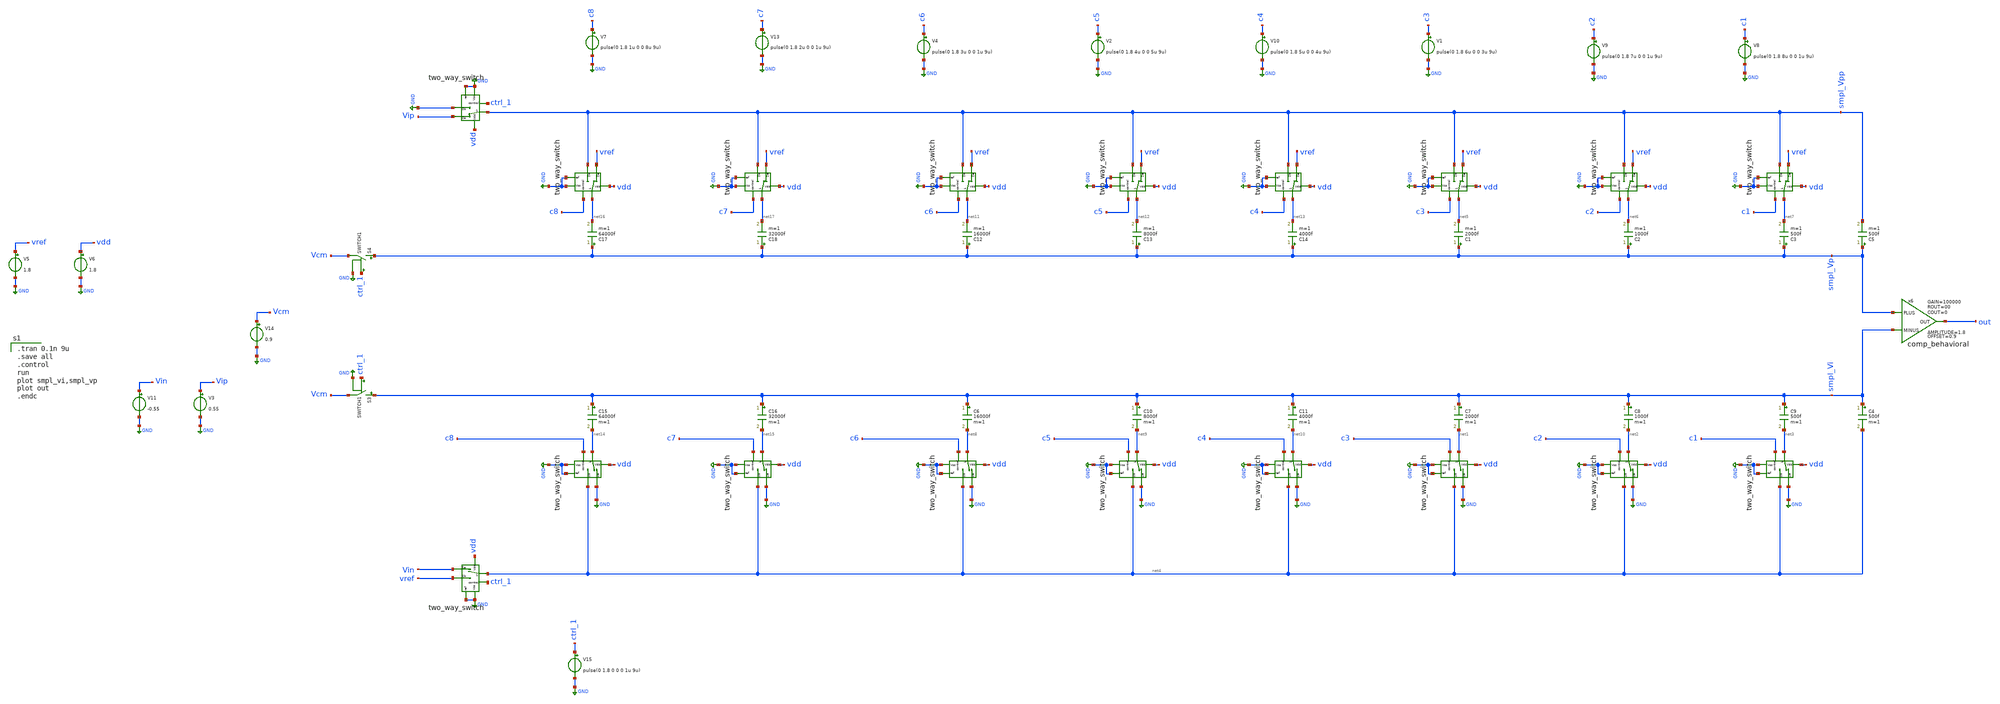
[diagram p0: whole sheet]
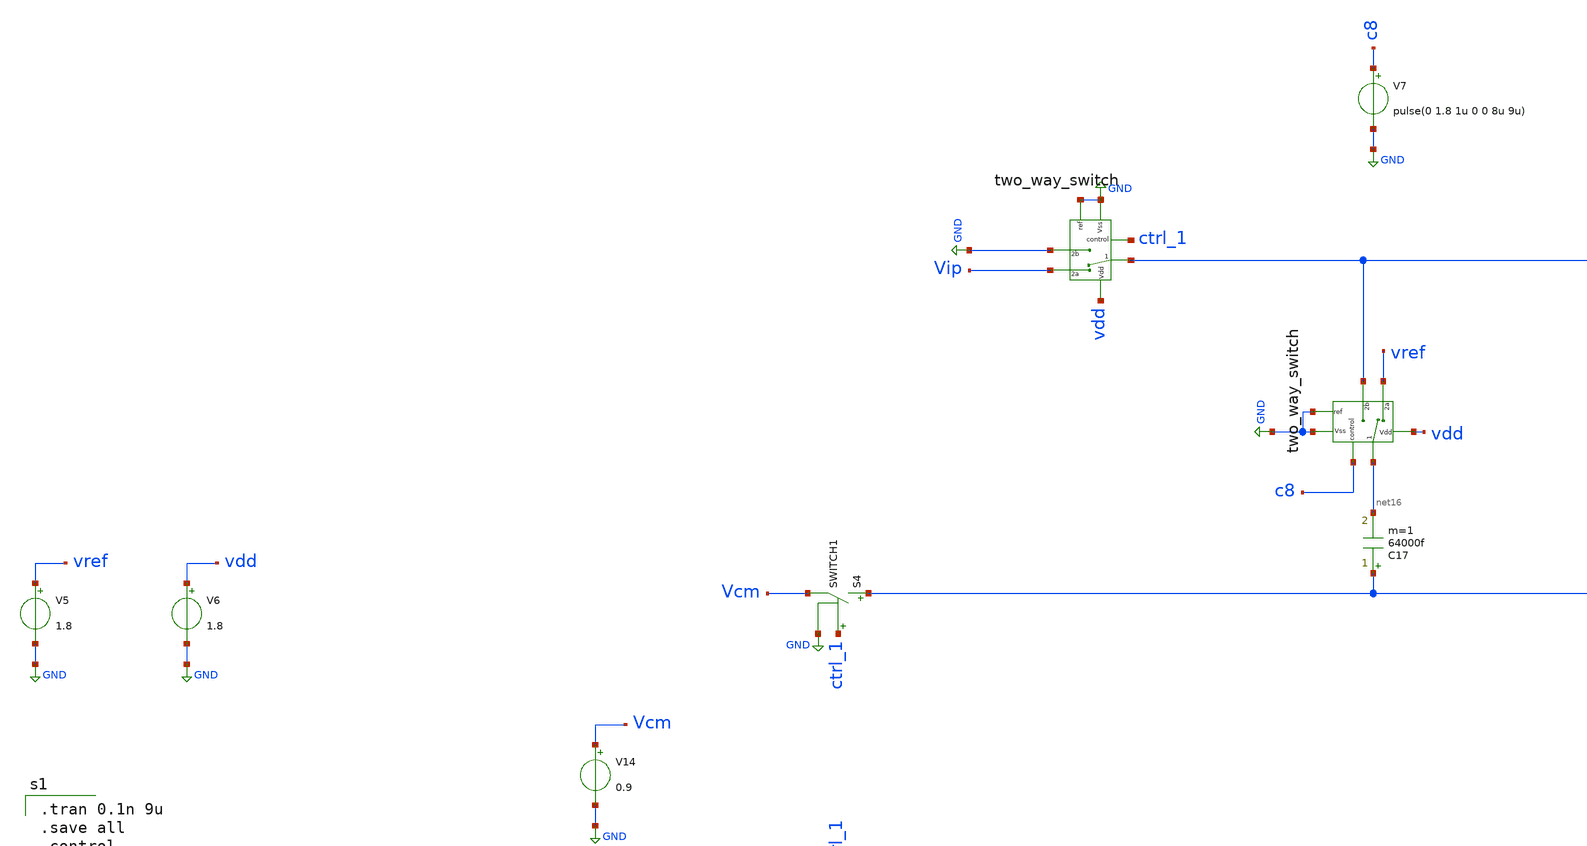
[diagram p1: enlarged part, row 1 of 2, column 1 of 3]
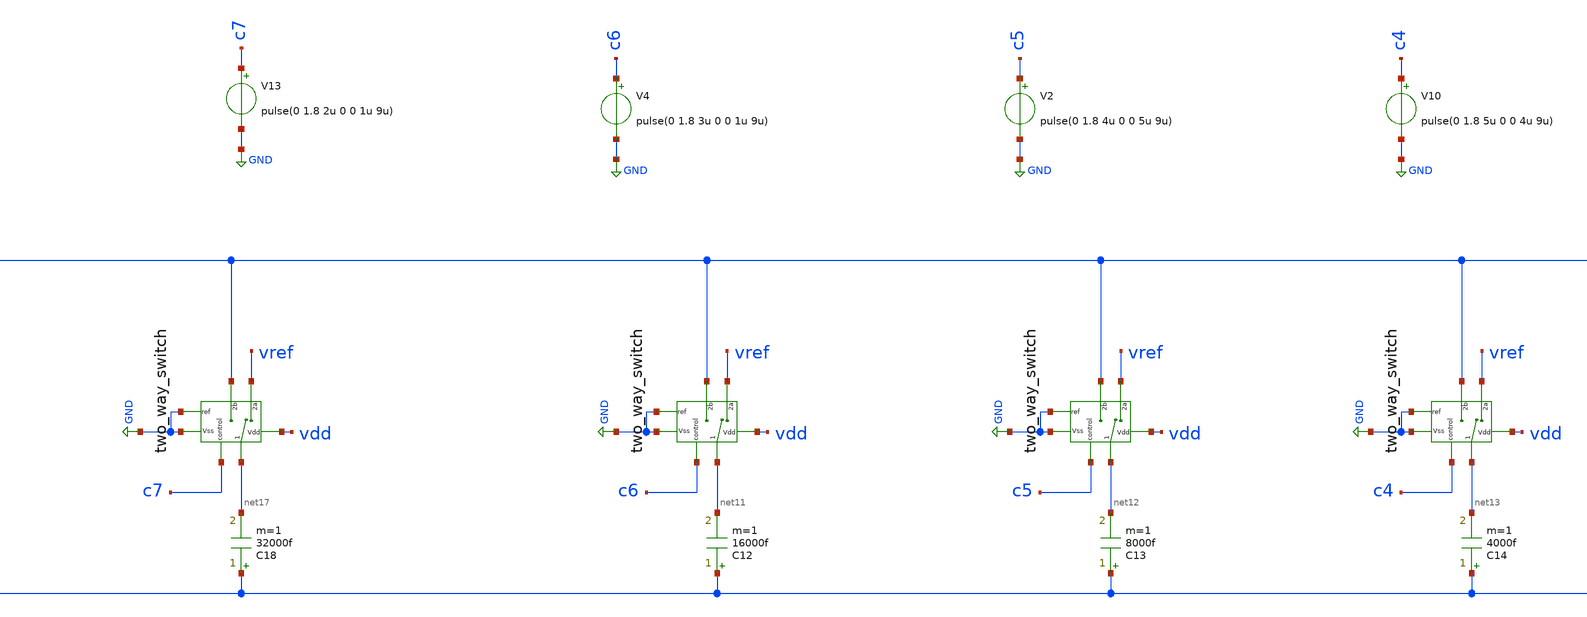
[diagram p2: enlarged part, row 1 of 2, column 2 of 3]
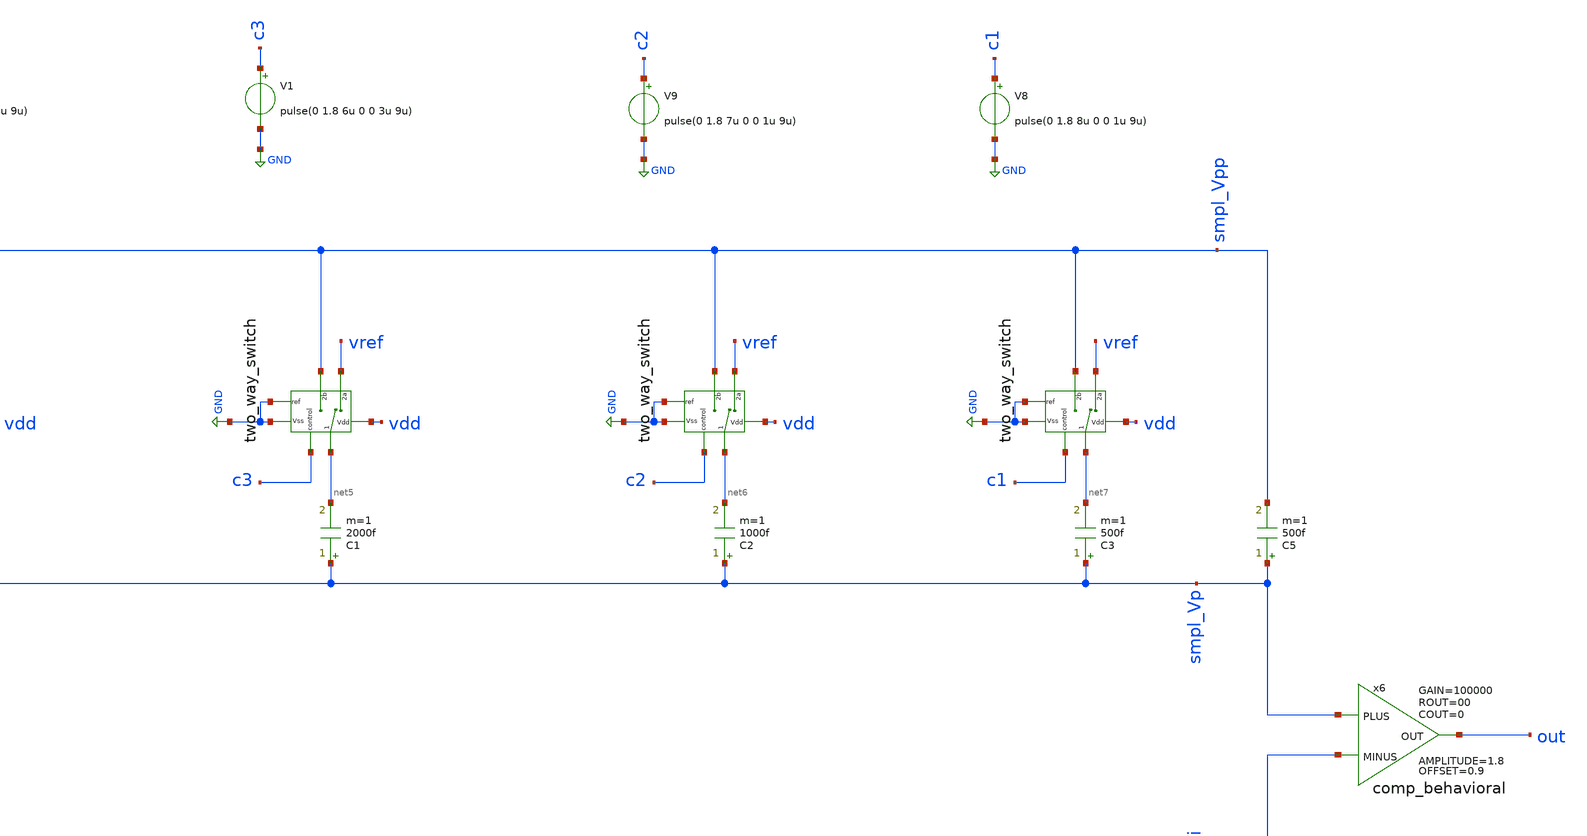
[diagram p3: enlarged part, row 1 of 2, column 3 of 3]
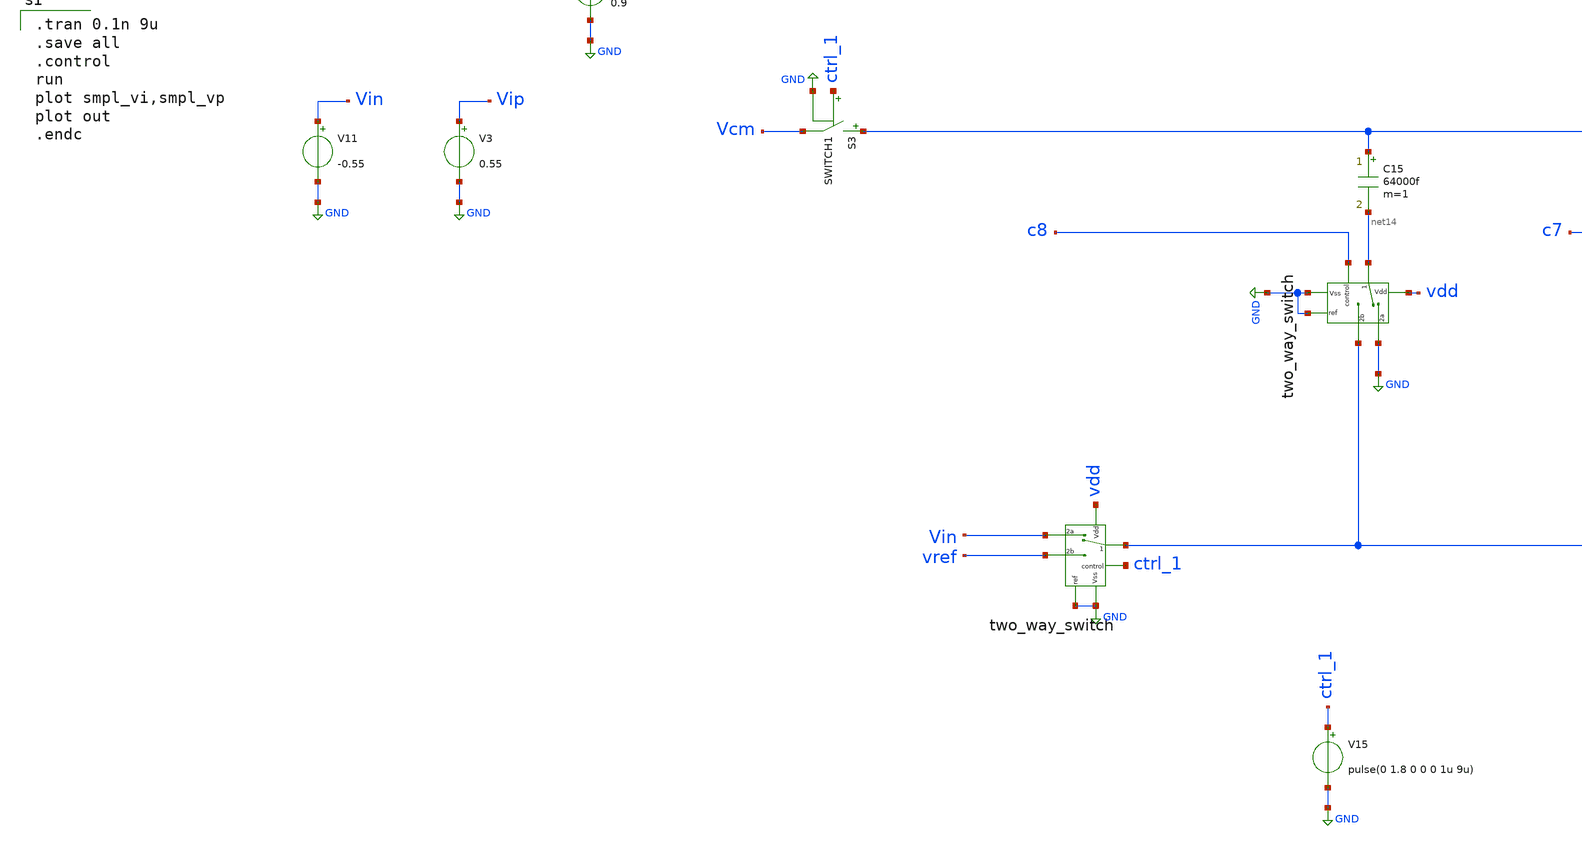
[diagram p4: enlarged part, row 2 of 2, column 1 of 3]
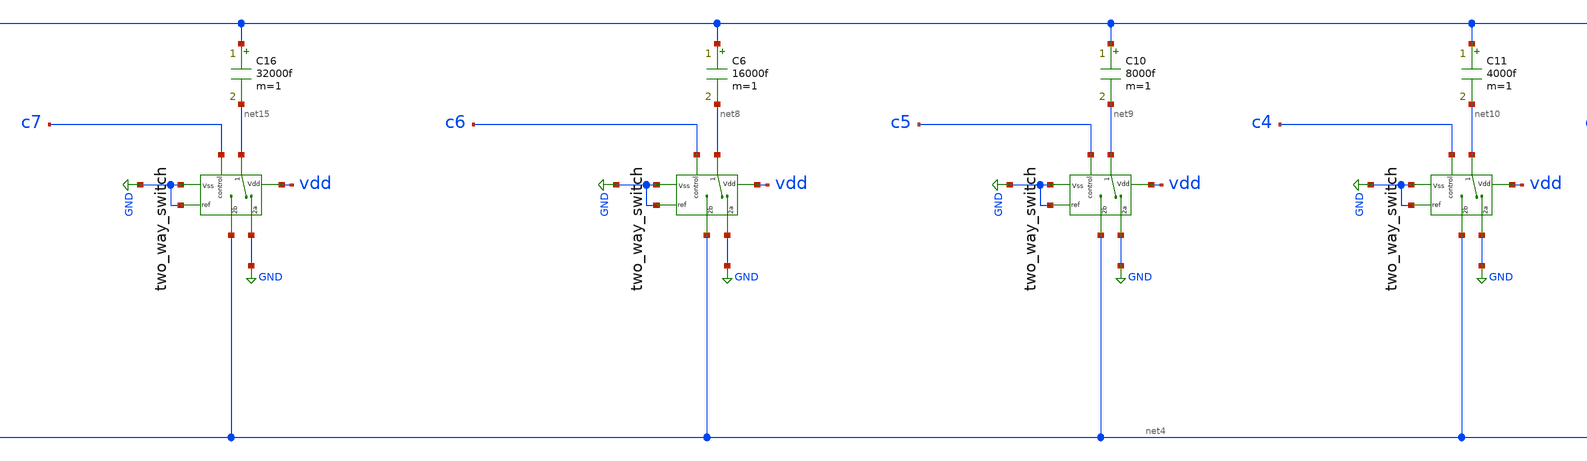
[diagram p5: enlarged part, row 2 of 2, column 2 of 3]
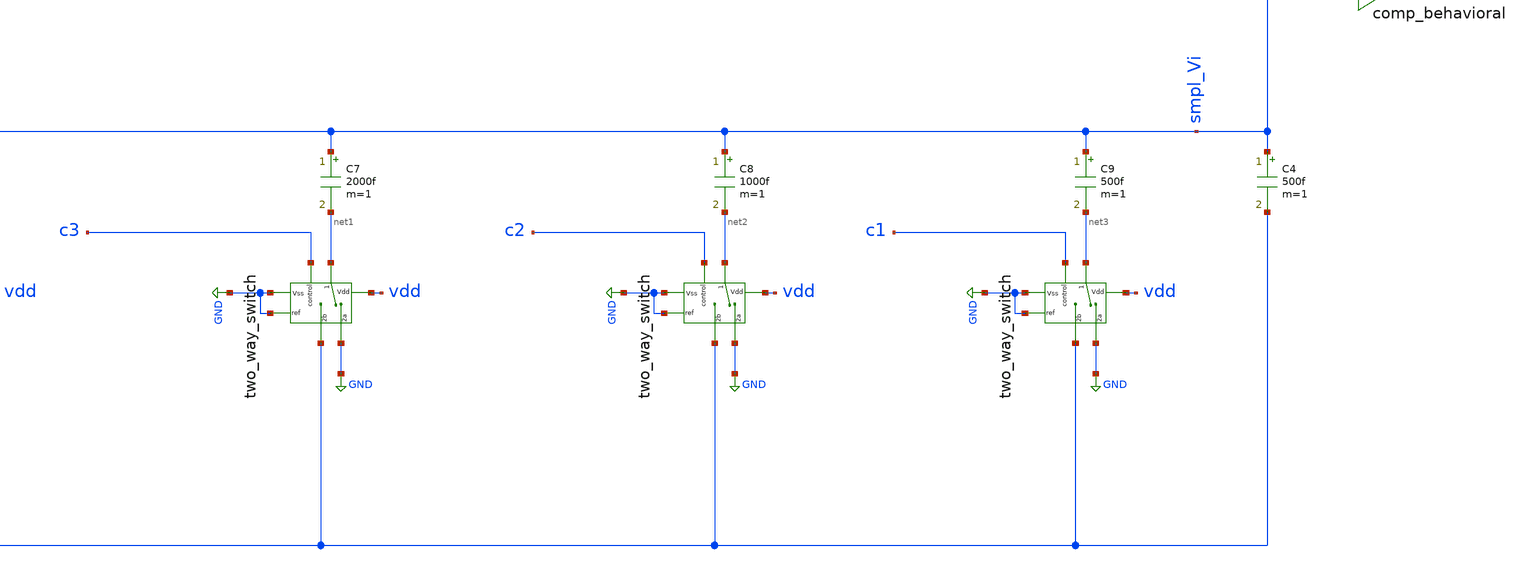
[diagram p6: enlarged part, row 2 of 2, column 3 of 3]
** sch_path: Behavioral_model/diff_mode_alternative_architecture.sch
**.subckt diff_mode_alternative_architecture
S3 smpl_Vi Vcm ctrl_1 GND SWITCH1
V3 Vip GND 0.55
C7 smpl_Vi net1 2000f m=1
x7 net1 vdd c3 GND GND net4 GND two_way_switch
C8 smpl_Vi net2 1000f m=1
C9 smpl_Vi net3 500f m=1
x1 net2 vdd c2 GND GND net4 GND two_way_switch
x2 net3 vdd c1 GND GND net4 GND two_way_switch
V5 vref GND 1.8
V6 vdd GND 1.8
S4 smpl_Vp Vcm ctrl_1 GND SWITCH1
C1 smpl_Vp net5 2000f m=1
x3 net5 vdd c3 GND vref smpl_Vpp GND two_way_switch
C2 smpl_Vp net6 1000f m=1
C3 smpl_Vp net7 500f m=1
x4 net6 vdd c2 GND vref smpl_Vpp GND two_way_switch
x5 net7 vdd c1 GND vref smpl_Vpp GND two_way_switch
V8 c1 GND pulse(0 1.8 8u 0 0 1u 9u)
V9 c2 GND pulse(0 1.8 7u 0 0 1u 9u)
V10 c4 GND pulse(0 1.8 5u 0 0 4u 9u)
x6 smpl_Vp smpl_Vi out comp_behavioral OFFSET=0.9 AMPLITUDE=1.8 GAIN=100000 ROUT=00 COUT=0
V11 Vin GND -0.55
C4 smpl_Vi net4 500f m=1
C5 smpl_Vp smpl_Vpp 500f m=1
C6 smpl_Vi net8 16000f m=1
x11 net8 vdd c6 GND GND net4 GND two_way_switch
C10 smpl_Vi net9 8000f m=1
C11 smpl_Vi net10 4000f m=1
x12 net9 vdd c5 GND GND net4 GND two_way_switch
x13 net10 vdd c4 GND GND net4 GND two_way_switch
C12 smpl_Vp net11 16000f m=1
x14 net11 vdd c6 GND vref smpl_Vpp GND two_way_switch
C13 smpl_Vp net12 8000f m=1
C14 smpl_Vp net13 4000f m=1
x15 net12 vdd c5 GND vref smpl_Vpp GND two_way_switch
x16 net13 vdd c4 GND vref smpl_Vpp GND two_way_switch
C15 smpl_Vi net14 64000f m=1
x20 net14 vdd c8 GND GND net4 GND two_way_switch
C16 smpl_Vi net15 32000f m=1
x21 net15 vdd c7 GND GND net4 GND two_way_switch
C17 smpl_Vp net16 64000f m=1
x22 net16 vdd c8 GND vref smpl_Vpp GND two_way_switch
C18 smpl_Vp net17 32000f m=1
x23 net17 vdd c7 GND vref smpl_Vpp GND two_way_switch
V1 c3 GND pulse(0 1.8 6u 0 0 3u 9u)
V2 c5 GND pulse(0 1.8 4u 0 0 5u 9u)
V4 c6 GND pulse(0 1.8 3u 0 0 1u 9u)
V7 c8 GND pulse(0 1.8 1u 0 0 8u 9u)
V13 c7 GND pulse(0 1.8 2u 0 0 1u 9u)
x26 smpl_Vpp vdd ctrl_1 GND Vip GND GND two_way_switch
x27 net4 vdd ctrl_1 GND Vin vref GND two_way_switch
V14 Vcm GND 0.9
V15 ctrl_1 GND pulse(0 1.8 0 0 0 1u 9u)
**** begin user architecture code

.tran 0.1n 9u
.save all
.control
run
plot smpl_vi,smpl_vp
plot out
.endc


.lib /usr/local/share/pdk/sky130A/libs.tech/ngspice/sky130.lib.spice tt


.model switch1 sw vt=0.1 vh=0 ron=1m roff=100G

**** end user architecture code
**.ends

* expanding   symbol:  two_way_switch.sym # of pins=7
** sym_path: Behavioral_model/two_way_switch.sym
** sch_path: Behavioral_model/two_way_switch.sch
.subckt two_way_switch 1 Vdd control ref 2a 2b Vss
*.iopin 2b
*.iopin 2a
*.ipin ref
*.iopin 1
*.ipin Vdd
*.ipin Vss
*.ipin control
S1 1 2a control ref SWITCH1
S2 1 2b net1 ref SWITCH1
x1 Vdd control net1 Vss CMOS_inverter
.ends


* expanding   symbol:  comp_behavioral.sym # of pins=3
** sym_path: Behavioral_model/comp_behavioral.sym
** sch_path: Behavioral_model/comp_behavioral.sch
.subckt comp_behavioral PLUS MINUS OUT  OFFSET=0.9 AMPLITUDE=0.9 GAIN=100000 ROUT=00 COUT=0
*.ipin PLUS
*.ipin MINUS
*.opin OUT
B1 IOUT 0 V = {OFFSET + AMPLITUDE/2*(tanh(V(IPLUS,IMINUS)*GAIN*2/AMPLITUDE))}
V1 IPLUS PLUS 3
V2 IMINUS MINUS 3
R1 OUT IOUT {ROUT} m=1
C3 OUT 0 {COUT} m=1
.ends


* expanding   symbol:  CMOS_inverter.sym # of pins=4
** sym_path: Behavioral_model/CMOS_inverter.sym
** sch_path: Behavioral_model/CMOS_inverter.sch
.subckt CMOS_inverter Vdd Q Q_N Vss
*.ipin Q
*.ipin Vdd
*.ipin Vss
*.opin Q_N
XM1 Q_N Q Vss Vss sky130_fd_pr__nfet_01v8 L=0.15 W=1 nf=1 ad='int((nf+1)/2) * W/nf * 0.29' as='int((nf+2)/2) * W/nf * 0.29'
+ pd='2*int((nf+1)/2) * (W/nf + 0.29)' ps='2*int((nf+2)/2) * (W/nf + 0.29)' nrd='0.29 / W' nrs='0.29 / W'
+ sa=0 sb=0 sd=0 mult=1 m=1
XM3 Q_N Q Vdd Vdd sky130_fd_pr__pfet_01v8 L=0.15 W=1 nf=1 ad='int((nf+1)/2) * W/nf * 0.29' as='int((nf+2)/2) * W/nf * 0.29'
+ pd='2*int((nf+1)/2) * (W/nf + 0.29)' ps='2*int((nf+2)/2) * (W/nf + 0.29)' nrd='0.29 / W' nrs='0.29 / W'
+ sa=0 sb=0 sd=0 mult=1 m=1
.ends

.GLOBAL GND
.end
